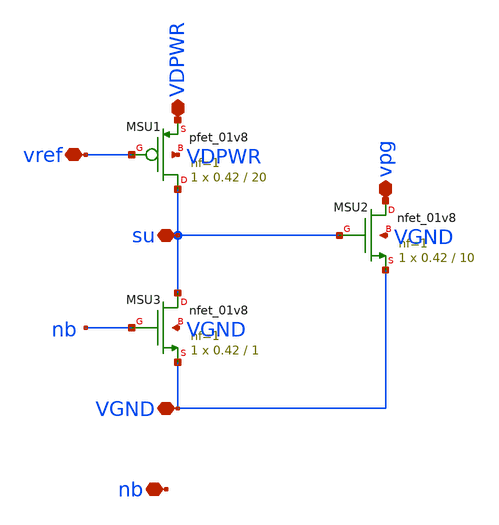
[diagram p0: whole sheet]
** sch_path: xschem/bg_su.sch
**.subckt bg_su vref VGND vpg VDPWR su nb
*.iopin vref
*.iopin VGND
*.iopin vpg
*.iopin VDPWR
*.iopin su
*.iopin nb
XMSU1 su vref VDPWR VDPWR sky130_fd_pr__pfet_01v8 L=20 W=0.42 nf=1 ad='int((1 + 1)/2) * 0.42 / 1 * 0.29'
+ as='int((1 + 2)/2) * 0.42 / 1 * 0.29' pd='2*int((1 + 1)/2) * (0.42 / 1 + 0.29)' ps='2*int((1 + 2)/2) * (0.42 / 1 + 0.29)'
+ nrd='0.29 / 0.42 ' nrs='0.29 / 0.42 ' sa=0 sb=0 sd=0 mult=1 m=1
XMSU3 su nb VGND VGND sky130_fd_pr__nfet_01v8 L=1 W=0.42 nf=1 ad='int((1 + 1)/2) * 0.42 / 1 * 0.29' as='int((1 + 2)/2) * 0.42 / 1 * 0.29'
+ pd='2*int((1 + 1)/2) * (0.42 / 1 + 0.29)' ps='2*int((1 + 2)/2) * (0.42 / 1 + 0.29)' nrd='0.29 / 0.42 '
+ nrs='0.29 / 0.42 ' sa=0 sb=0 sd=0 mult=1 m=1
XMSU2 vpg su VGND VGND sky130_fd_pr__nfet_01v8 L=10 W=0.42 nf=1 ad='int((1 + 1)/2) * 0.42 / 1 * 0.29'
+ as='int((1 + 2)/2) * 0.42 / 1 * 0.29' pd='2*int((1 + 1)/2) * (0.42 / 1 + 0.29)' ps='2*int((1 + 2)/2) * (0.42 / 1 + 0.29)'
+ nrd='0.29 / 0.42 ' nrs='0.29 / 0.42 ' sa=0 sb=0 sd=0 mult=1 m=1
**.ends
.end
